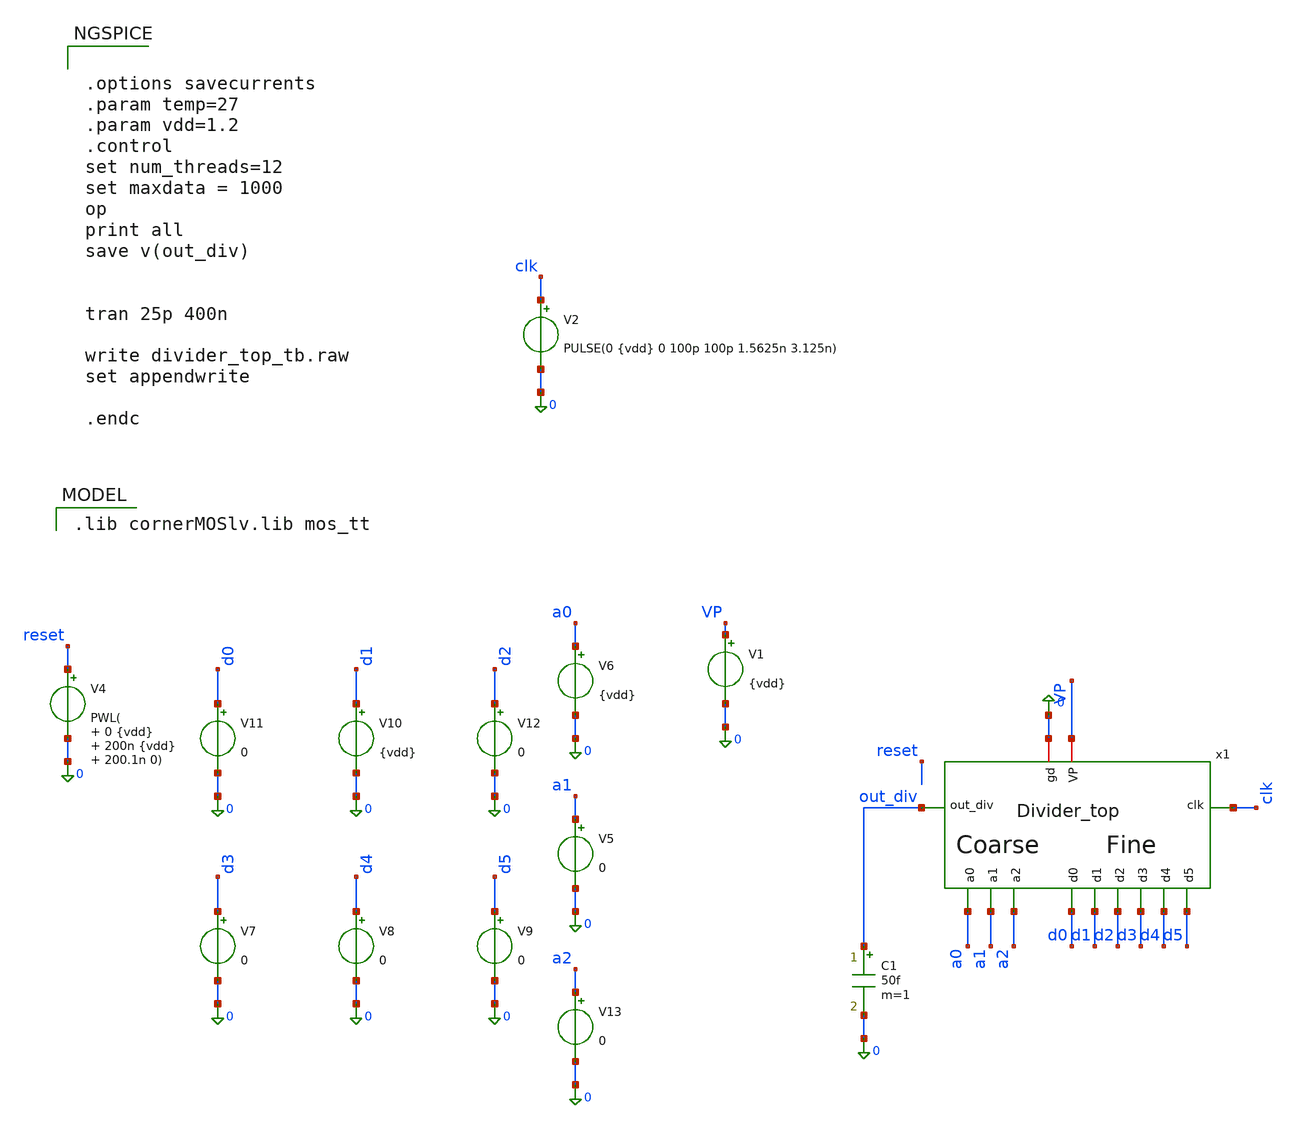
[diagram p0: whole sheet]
** sch_path: PLL0663-main/testbenches/tran/xschem/divider/divider_top_tb.sch
**.subckt divider_top_tb
V1 VP 0 {vdd}
V2 clk 0 PULSE(0 {vdd} 0 100p 100p 1.5625n 3.125n)
V8 d4 0 0
V9 d5 0 0
V11 d0 0 0
V10 d1 0 {vdd}
V12 d2 0 0
V7 d3 0 0
V5 a1 0 0
V6 a0 0 {vdd}
V13 a2 0 0
x1 0 VP clk d0 d1 d2 d3 d4 d5 a0 a1 a2 out_div Divider_top
V4 reset 0 PWL( 0 {vdd} 200n {vdd} 200.1n 0)
C1 out_div 0 50f m=1
**** begin user architecture code


.options savecurrents
.param temp=27
.param vdd=1.2
.control
set num_threads=12
set maxdata = 1000
op
print all
save v(out_div)


tran 25p 400n

write divider_top_tb.raw
set appendwrite

.endc


 .lib cornerMOSlv.lib mos_tt

**** end user architecture code
**.ends
.end
